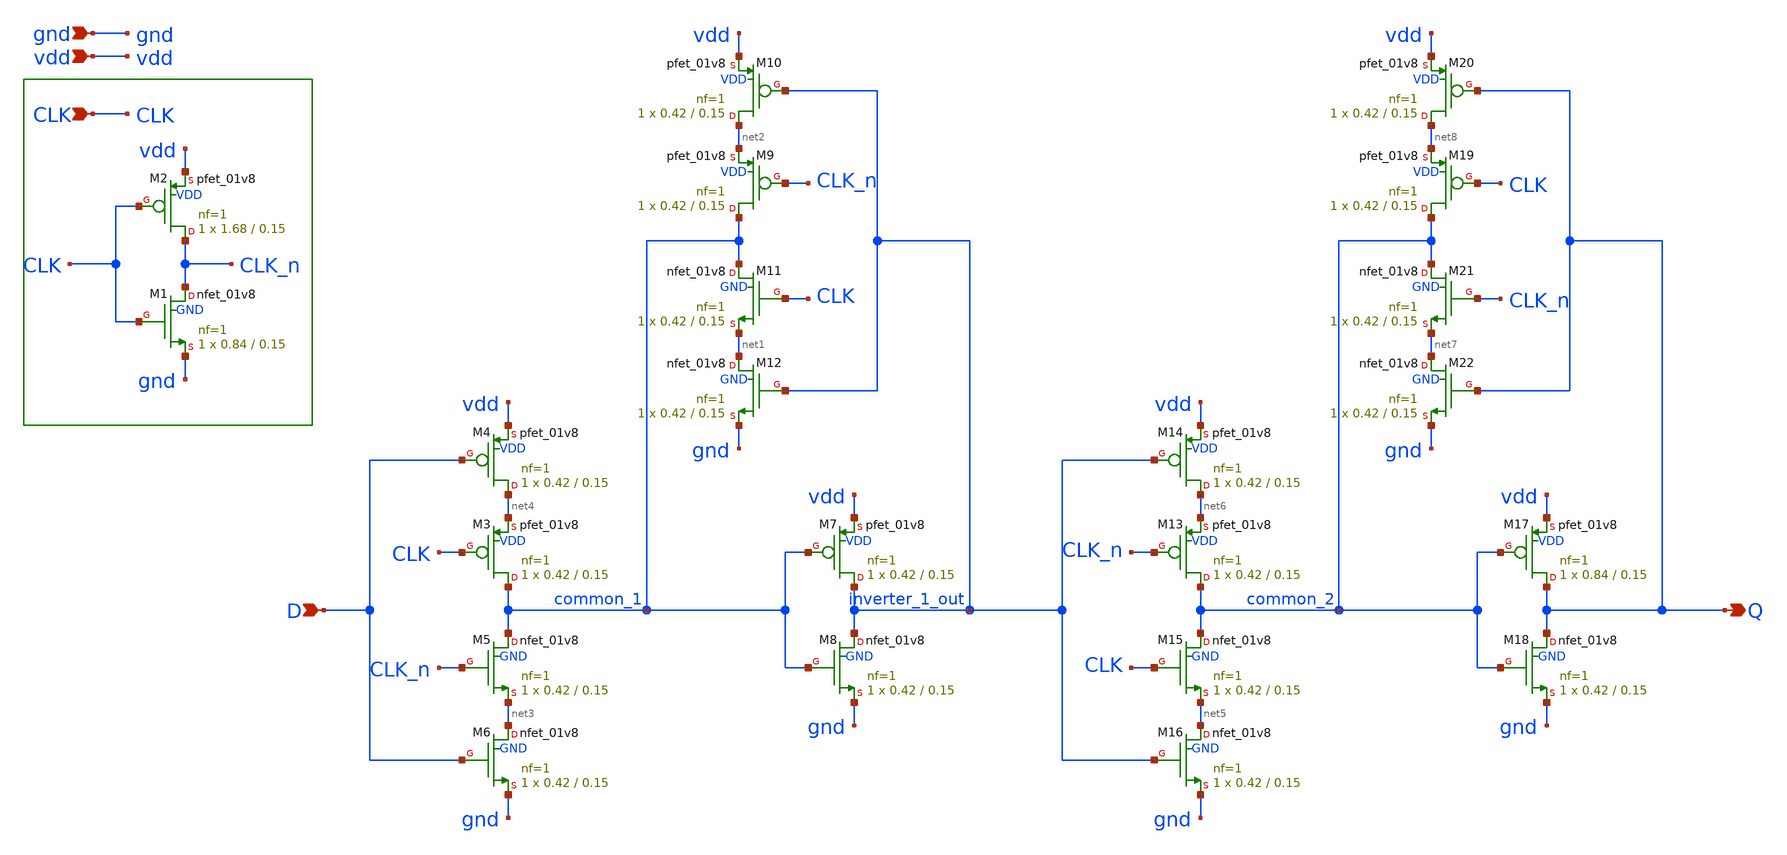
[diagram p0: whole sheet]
** sch_path: xschem/d_flip_flop.sch
**.subckt d_flip_flop CLK D Q vdd gnd
*.ipin CLK
*.ipin D
*.opin Q
*.ipin vdd
*.ipin gnd
XM1 CLK_n CLK gnd GND sky130_fd_pr__nfet_01v8 L=0.15 W=0.84 nf=1 ad='int((nf+1)/2) * W/nf * 0.29' as='int((nf+2)/2) * W/nf * 0.29'
+ pd='2*int((nf+1)/2) * (W/nf + 0.29)' ps='2*int((nf+2)/2) * (W/nf + 0.29)' nrd='0.29 / W' nrs='0.29 / W'
+ sa=0 sb=0 sd=0 mult=1 m=1
XM2 CLK_n CLK vdd VDD sky130_fd_pr__pfet_01v8 L=0.15 W=1.68 nf=1 ad='int((nf+1)/2) * W/nf * 0.29' as='int((nf+2)/2) * W/nf * 0.29'
+ pd='2*int((nf+1)/2) * (W/nf + 0.29)' ps='2*int((nf+2)/2) * (W/nf + 0.29)' nrd='0.29 / W' nrs='0.29 / W'
+ sa=0 sb=0 sd=0 mult=1 m=1
XM3 common_1 CLK net4 VDD sky130_fd_pr__pfet_01v8 L=0.15 W=0.42 nf=1 ad='int((nf+1)/2) * W/nf * 0.29'
+ as='int((nf+2)/2) * W/nf * 0.29' pd='2*int((nf+1)/2) * (W/nf + 0.29)' ps='2*int((nf+2)/2) * (W/nf + 0.29)'
+ nrd='0.29 / W' nrs='0.29 / W' sa=0 sb=0 sd=0 mult=1 m=1
XM4 net4 D vdd VDD sky130_fd_pr__pfet_01v8 L=0.15 W=0.42 nf=1 ad='int((nf+1)/2) * W/nf * 0.29' as='int((nf+2)/2) * W/nf * 0.29'
+ pd='2*int((nf+1)/2) * (W/nf + 0.29)' ps='2*int((nf+2)/2) * (W/nf + 0.29)' nrd='0.29 / W' nrs='0.29 / W'
+ sa=0 sb=0 sd=0 mult=1 m=1
XM5 common_1 CLK_n net3 GND sky130_fd_pr__nfet_01v8 L=0.15 W=0.42 nf=1 ad='int((nf+1)/2) * W/nf * 0.29'
+ as='int((nf+2)/2) * W/nf * 0.29' pd='2*int((nf+1)/2) * (W/nf + 0.29)' ps='2*int((nf+2)/2) * (W/nf + 0.29)'
+ nrd='0.29 / W' nrs='0.29 / W' sa=0 sb=0 sd=0 mult=1 m=1
XM6 net3 D gnd GND sky130_fd_pr__nfet_01v8 L=0.15 W=0.42 nf=1 ad='int((nf+1)/2) * W/nf * 0.29' as='int((nf+2)/2) * W/nf * 0.29'
+ pd='2*int((nf+1)/2) * (W/nf + 0.29)' ps='2*int((nf+2)/2) * (W/nf + 0.29)' nrd='0.29 / W' nrs='0.29 / W'
+ sa=0 sb=0 sd=0 mult=1 m=1
XM7 inverter_1_out common_1 vdd VDD sky130_fd_pr__pfet_01v8 L=0.15 W=0.42 nf=1 ad='int((nf+1)/2) * W/nf * 0.29'
+ as='int((nf+2)/2) * W/nf * 0.29' pd='2*int((nf+1)/2) * (W/nf + 0.29)' ps='2*int((nf+2)/2) * (W/nf + 0.29)'
+ nrd='0.29 / W' nrs='0.29 / W' sa=0 sb=0 sd=0 mult=1 m=1
XM8 inverter_1_out common_1 gnd GND sky130_fd_pr__nfet_01v8 L=0.15 W=0.42 nf=1 ad='int((nf+1)/2) * W/nf * 0.29'
+ as='int((nf+2)/2) * W/nf * 0.29' pd='2*int((nf+1)/2) * (W/nf + 0.29)' ps='2*int((nf+2)/2) * (W/nf + 0.29)'
+ nrd='0.29 / W' nrs='0.29 / W' sa=0 sb=0 sd=0 mult=1 m=1
XM9 common_1 CLK_n net2 VDD sky130_fd_pr__pfet_01v8 L=0.15 W=0.42 nf=1 ad='int((nf+1)/2) * W/nf * 0.29'
+ as='int((nf+2)/2) * W/nf * 0.29' pd='2*int((nf+1)/2) * (W/nf + 0.29)' ps='2*int((nf+2)/2) * (W/nf + 0.29)'
+ nrd='0.29 / W' nrs='0.29 / W' sa=0 sb=0 sd=0 mult=1 m=1
XM10 net2 inverter_1_out vdd VDD sky130_fd_pr__pfet_01v8 L=0.15 W=0.42 nf=1 ad='int((nf+1)/2) * W/nf * 0.29'
+ as='int((nf+2)/2) * W/nf * 0.29' pd='2*int((nf+1)/2) * (W/nf + 0.29)' ps='2*int((nf+2)/2) * (W/nf + 0.29)'
+ nrd='0.29 / W' nrs='0.29 / W' sa=0 sb=0 sd=0 mult=1 m=1
XM11 common_1 CLK net1 GND sky130_fd_pr__nfet_01v8 L=0.15 W=0.42 nf=1 ad='int((nf+1)/2) * W/nf * 0.29'
+ as='int((nf+2)/2) * W/nf * 0.29' pd='2*int((nf+1)/2) * (W/nf + 0.29)' ps='2*int((nf+2)/2) * (W/nf + 0.29)'
+ nrd='0.29 / W' nrs='0.29 / W' sa=0 sb=0 sd=0 mult=1 m=1
XM12 net1 inverter_1_out gnd GND sky130_fd_pr__nfet_01v8 L=0.15 W=0.42 nf=1 ad='int((nf+1)/2) * W/nf * 0.29'
+ as='int((nf+2)/2) * W/nf * 0.29' pd='2*int((nf+1)/2) * (W/nf + 0.29)' ps='2*int((nf+2)/2) * (W/nf + 0.29)'
+ nrd='0.29 / W' nrs='0.29 / W' sa=0 sb=0 sd=0 mult=1 m=1
XM13 common_2 CLK_n net6 VDD sky130_fd_pr__pfet_01v8 L=0.15 W=0.42 nf=1 ad='int((nf+1)/2) * W/nf * 0.29'
+ as='int((nf+2)/2) * W/nf * 0.29' pd='2*int((nf+1)/2) * (W/nf + 0.29)' ps='2*int((nf+2)/2) * (W/nf + 0.29)'
+ nrd='0.29 / W' nrs='0.29 / W' sa=0 sb=0 sd=0 mult=1 m=1
XM14 net6 inverter_1_out vdd VDD sky130_fd_pr__pfet_01v8 L=0.15 W=0.42 nf=1 ad='int((nf+1)/2) * W/nf * 0.29'
+ as='int((nf+2)/2) * W/nf * 0.29' pd='2*int((nf+1)/2) * (W/nf + 0.29)' ps='2*int((nf+2)/2) * (W/nf + 0.29)'
+ nrd='0.29 / W' nrs='0.29 / W' sa=0 sb=0 sd=0 mult=1 m=1
XM15 common_2 CLK net5 GND sky130_fd_pr__nfet_01v8 L=0.15 W=0.42 nf=1 ad='int((nf+1)/2) * W/nf * 0.29'
+ as='int((nf+2)/2) * W/nf * 0.29' pd='2*int((nf+1)/2) * (W/nf + 0.29)' ps='2*int((nf+2)/2) * (W/nf + 0.29)'
+ nrd='0.29 / W' nrs='0.29 / W' sa=0 sb=0 sd=0 mult=1 m=1
XM16 net5 inverter_1_out gnd GND sky130_fd_pr__nfet_01v8 L=0.15 W=0.42 nf=1 ad='int((nf+1)/2) * W/nf * 0.29'
+ as='int((nf+2)/2) * W/nf * 0.29' pd='2*int((nf+1)/2) * (W/nf + 0.29)' ps='2*int((nf+2)/2) * (W/nf + 0.29)'
+ nrd='0.29 / W' nrs='0.29 / W' sa=0 sb=0 sd=0 mult=1 m=1
XM17 Q common_2 vdd VDD sky130_fd_pr__pfet_01v8 L=0.15 W=0.84 nf=1 ad='int((nf+1)/2) * W/nf * 0.29' as='int((nf+2)/2) * W/nf * 0.29'
+ pd='2*int((nf+1)/2) * (W/nf + 0.29)' ps='2*int((nf+2)/2) * (W/nf + 0.29)' nrd='0.29 / W' nrs='0.29 / W'
+ sa=0 sb=0 sd=0 mult=1 m=1
XM18 Q common_2 gnd GND sky130_fd_pr__nfet_01v8 L=0.15 W=0.42 nf=1 ad='int((nf+1)/2) * W/nf * 0.29' as='int((nf+2)/2) * W/nf * 0.29'
+ pd='2*int((nf+1)/2) * (W/nf + 0.29)' ps='2*int((nf+2)/2) * (W/nf + 0.29)' nrd='0.29 / W' nrs='0.29 / W'
+ sa=0 sb=0 sd=0 mult=1 m=1
XM19 common_2 CLK net8 VDD sky130_fd_pr__pfet_01v8 L=0.15 W=0.42 nf=1 ad='int((nf+1)/2) * W/nf * 0.29'
+ as='int((nf+2)/2) * W/nf * 0.29' pd='2*int((nf+1)/2) * (W/nf + 0.29)' ps='2*int((nf+2)/2) * (W/nf + 0.29)'
+ nrd='0.29 / W' nrs='0.29 / W' sa=0 sb=0 sd=0 mult=1 m=1
XM20 net8 Q vdd VDD sky130_fd_pr__pfet_01v8 L=0.15 W=0.42 nf=1 ad='int((nf+1)/2) * W/nf * 0.29' as='int((nf+2)/2) * W/nf * 0.29'
+ pd='2*int((nf+1)/2) * (W/nf + 0.29)' ps='2*int((nf+2)/2) * (W/nf + 0.29)' nrd='0.29 / W' nrs='0.29 / W'
+ sa=0 sb=0 sd=0 mult=1 m=1
XM21 common_2 CLK_n net7 GND sky130_fd_pr__nfet_01v8 L=0.15 W=0.42 nf=1 ad='int((nf+1)/2) * W/nf * 0.29'
+ as='int((nf+2)/2) * W/nf * 0.29' pd='2*int((nf+1)/2) * (W/nf + 0.29)' ps='2*int((nf+2)/2) * (W/nf + 0.29)'
+ nrd='0.29 / W' nrs='0.29 / W' sa=0 sb=0 sd=0 mult=1 m=1
XM22 net7 Q gnd GND sky130_fd_pr__nfet_01v8 L=0.15 W=0.42 nf=1 ad='int((nf+1)/2) * W/nf * 0.29' as='int((nf+2)/2) * W/nf * 0.29'
+ pd='2*int((nf+1)/2) * (W/nf + 0.29)' ps='2*int((nf+2)/2) * (W/nf + 0.29)' nrd='0.29 / W' nrs='0.29 / W'
+ sa=0 sb=0 sd=0 mult=1 m=1
**.ends
.end
